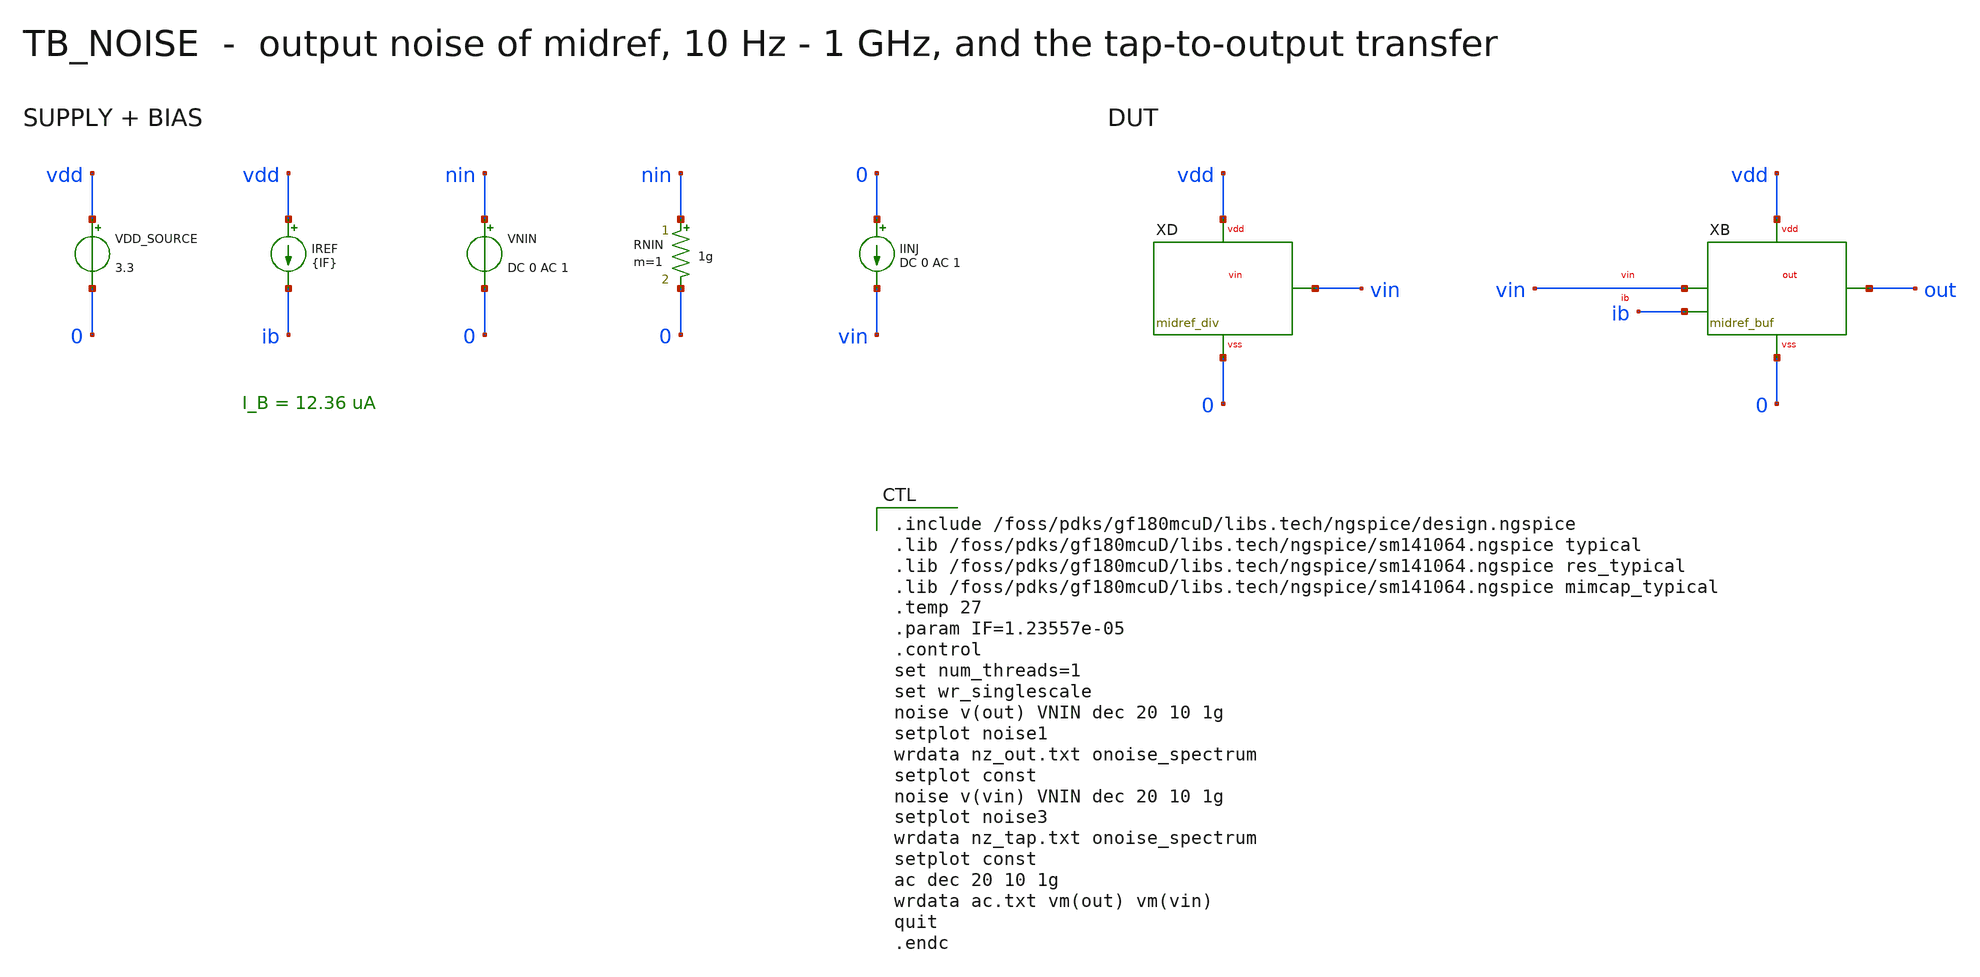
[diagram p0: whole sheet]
** sch_path: mixed_signal/midrail_ref/tb_noise.sch
**.subckt tb_noise
VDD_SOURCE vdd 0 3.3
IREF vdd ib {IF}
VNIN nin 0 DC 0 AC 1
RNIN nin 0 1g m=1
IINJ 0 vin DC 0 AC 1
XD vin vdd 0 midref_div
XB out vin ib vdd 0 midref_buf
**** begin user architecture code

.include /foss/pdks/gf180mcuD/libs.tech/ngspice/design.ngspice
.lib /foss/pdks/gf180mcuD/libs.tech/ngspice/sm141064.ngspice typical
.lib /foss/pdks/gf180mcuD/libs.tech/ngspice/sm141064.ngspice res_typical
.lib /foss/pdks/gf180mcuD/libs.tech/ngspice/sm141064.ngspice mimcap_typical
.temp 27
.param IF=1.23557e-05
.control
set num_threads=1
set wr_singlescale
noise v(out) VNIN dec 20 10 1g
setplot noise1
wrdata nz_out.txt onoise_spectrum
setplot const
noise v(vin) VNIN dec 20 10 1g
setplot noise3
wrdata nz_tap.txt onoise_spectrum
setplot const
ac dec 20 10 1g
wrdata ac.txt vm(out) vm(vin)
quit
.endc

**** end user architecture code
**.ends
.end
